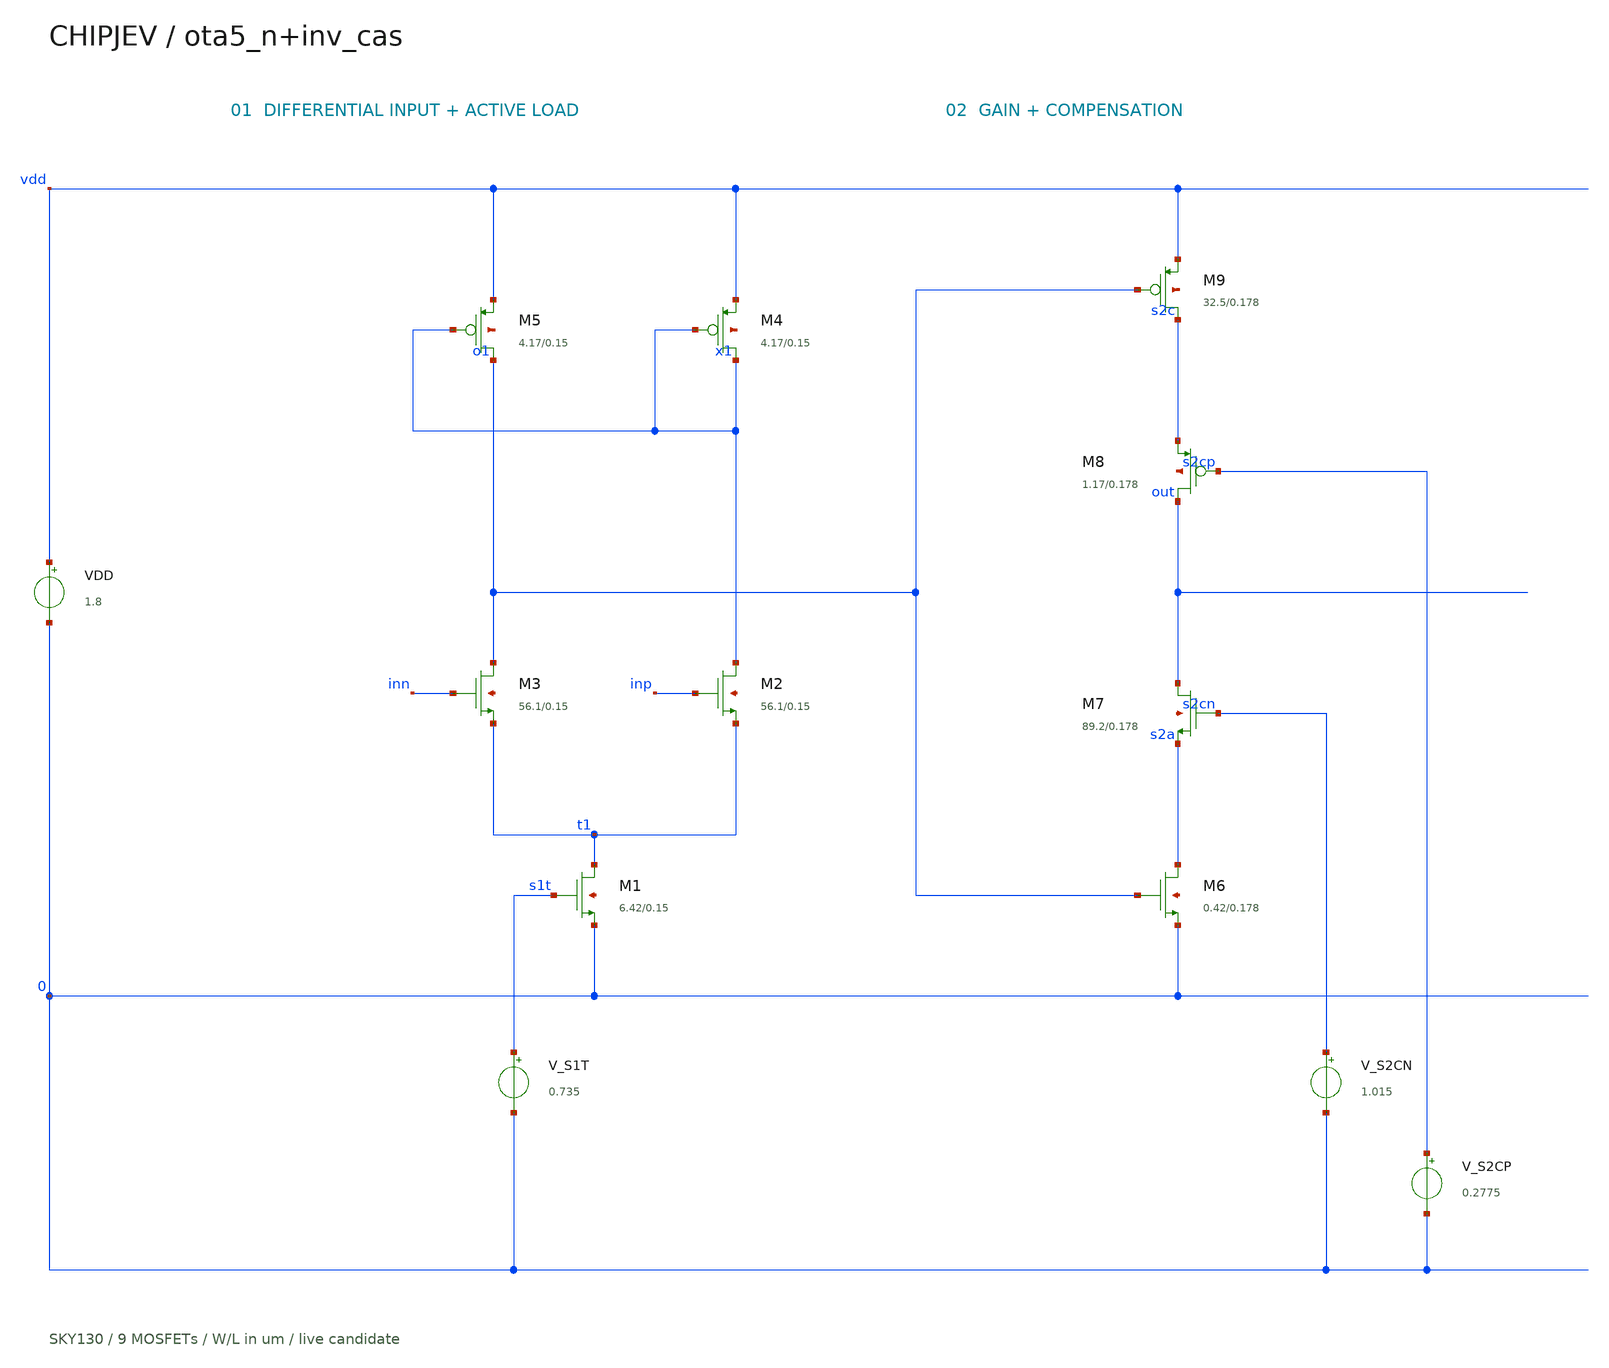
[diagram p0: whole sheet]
** sch_path: experiments/layout/results/opamp-speed/circuit.sch
**.subckt circuit
VDD vdd 0 1.8
XM1 t1 s1t 0 0 sky130_fd_pr__nfet_01v8 L=0.15 W=6.42 nf=1 ad=1.8618 as=1.8618 pd=13.42 ps=13.42
+ nrd=0.0451713 nrs=0.0451713 sa=0 sb=0 sd=0 mult=1 m=1
XM2 x1 inp t1 0 sky130_fd_pr__nfet_01v8 L=0.15 W=56.1 nf=2 ad=8.1345 as=16.269 pd=56.68 ps=113.36
+ nrd=0.00516934 nrs=0.00516934 sa=0 sb=0 sd=0 mult=1 m=1
XM3 o1 inn t1 0 sky130_fd_pr__nfet_01v8 L=0.15 W=56.1 nf=2 ad=8.1345 as=16.269 pd=56.68 ps=113.36
+ nrd=0.00516934 nrs=0.00516934 sa=0 sb=0 sd=0 mult=1 m=1
XM4 x1 x1 vdd vdd sky130_fd_pr__pfet_01v8 L=0.15 W=4.17 nf=1 ad=1.2093 as=1.2093 pd=8.92 ps=8.92
+ nrd=0.0695444 nrs=0.0695444 sa=0 sb=0 sd=0 mult=1 m=1
XM5 o1 x1 vdd vdd sky130_fd_pr__pfet_01v8 L=0.15 W=4.17 nf=1 ad=1.2093 as=1.2093 pd=8.92 ps=8.92
+ nrd=0.0695444 nrs=0.0695444 sa=0 sb=0 sd=0 mult=1 m=1
XM6 s2a o1 0 0 sky130_fd_pr__nfet_01v8 L=0.178333 W=0.42 nf=1 ad=0.1218 as=0.1218 pd=1.42 ps=1.42
+ nrd=0.690476 nrs=0.690476 sa=0 sb=0 sd=0 mult=1 m=1
XM7 out s2cn s2a 0 sky130_fd_pr__nfet_01v8 L=0.178333 W=89.1667 nf=2 ad=12.9292 as=25.8583
+ pd=89.7467 ps=179.493 nrd=0.00325234 nrs=0.00325234 sa=0 sb=0 sd=0 mult=1 m=1
XM8 out s2cp s2c vdd sky130_fd_pr__pfet_01v8 L=0.178333 W=1.16808 nf=1 ad=0.338744 as=0.338744
+ pd=2.91617 ps=2.91617 nrd=0.24827 nrs=0.24827 sa=0 sb=0 sd=0 mult=1 m=1
XM9 s2c o1 vdd vdd sky130_fd_pr__pfet_01v8 L=0.178333 W=32.4567 nf=1 ad=9.41243 as=9.41243
+ pd=65.4933 ps=65.4933 nrd=0.00893499 nrs=0.00893499 sa=0 sb=0 sd=0 mult=1 m=1
V_S1T s1t 0 0.735
V_S2CN s2cn 0 1.015
V_S2CP s2cp 0 0.2775
**.ends
.end
